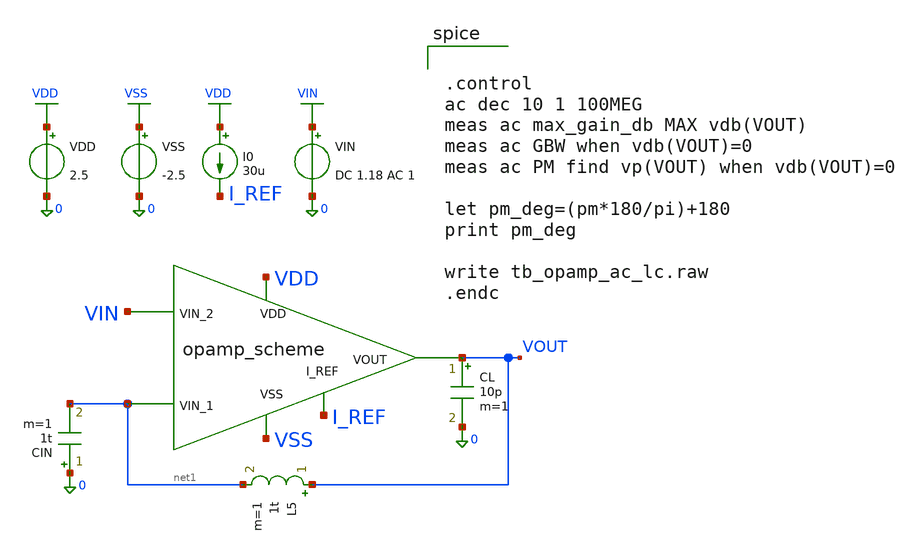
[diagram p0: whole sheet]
** sch_path: schematic/tb_opamp_ac_lc.sch
**.subckt tb_opamp_ac_lc
x1 VDD I_REF VOUT VIN net1 VSS opamp_scheme
VDD VDD 0 2.5
VSS VSS 0 -2.5
I0 VDD I_REF 30u
CL VOUT 0 10p m=1
VIN VIN 0 DC 1.18 AC 1
CIN 0 net1 1t m=1
L5 VOUT net1 1t m=1
**** begin user architecture code

.MODEL N_1u NMOS LEVEL  = 3
  TOX    = 200E-10         NSUB   = 1E17            GAMMA  = 0.5
  PHI    = 0.7             VTO    = 0.8             DELTA  = 3.0
  UO     = 650             ETA    = 3.0E-6          THETA  = 0.1
  KP     = 120E-6          VMAX   = 1E5             KAPPA  = 0.3
  RSH    = 0               NFS    = 1E12            TPG    = 1
  XJ     = 500E-9          LD     = 100E-9
  CGDO   = 200E-12         CGSO   = 200E-12         CGBO   = 1E-10
  CJ     = 400E-6          PB     = 1               MJ     = 0.5
  CJSW   = 300E-12         MJSW   = 0.5

*

.MODEL P_1u PMOS LEVEL  = 3
  TOX    = 200E-10         NSUB   = 1E17            GAMMA  = 0.6
  PHI    = 0.7             VTO    = -0.9            DELTA  = 0.1
  UO     = 250             ETA    = 0               THETA  = 0.1
  KP     = 40E-6           VMAX   = 5E4             KAPPA  = 1
  RSH    = 0               NFS    = 1E12            TPG    = -1
  XJ     = 500E-9          LD     = 100E-9
  CGDO   = 200E-12         CGSO   = 200E-12         CGBO   = 1E-10
  CJ     = 400E-6          PB     = 1               MJ     = 0.5
  CJSW   = 300E-12         MJSW   = 0.5



.param L=1u W1=3.5u W2=3.5u W3=10u W4=10u W5=3u W6=86.6u W7=13u W8=3u Cc=2.5p




.control
ac dec 10 1 100MEG
meas ac max_gain_db MAX vdb(VOUT)
meas ac GBW when vdb(VOUT)=0
meas ac PM find vp(VOUT) when vdb(VOUT)=0

let pm_deg=(pm*180/pi)+180
print pm_deg

write tb_opamp_ac_lc.raw
.endc


**** end user architecture code
**.ends

* expanding   symbol:  opamp_scheme.sym # of pins=6
** sym_path: schematic/opamp_scheme.sym
** sch_path: schematic/opamp_scheme.sch
.subckt opamp_scheme VDD I_REF VOUT VIN_2 VIN_1 VSS
*.opin VOUT
*.ipin VIN_1
*.ipin VIN_2
*.ipin I_REF
*.ipin VDD
*.ipin VSS
V1 I_REF VBIAS 0
C1 net3 VOUT {Cc} m=1
M1 net1 VIN_1 net2 VSS N_1u w=W1 l=L m=1
M2 net3 VIN_2 net2 VSS N_1u w=W2 l=L m=1
M3 net1 net1 VDD VDD P_1u w=W3 l=L m=1
M4 net3 net1 VDD VDD P_1u w=W4 l=L m=1
M5 net2 VBIAS VSS VSS N_1u w=W5 l=L m=1
M6 VOUT net3 VDD VDD P_1u w=W6 l=L m=1
M7 VOUT VBIAS VSS VSS N_1u w=W7 l=L m=1
M8 VBIAS VBIAS VSS VSS N_1u w=W8 l=L m=1
.ends

.GLOBAL VDD
.GLOBAL VSS
.GLOBAL VIN
.end
